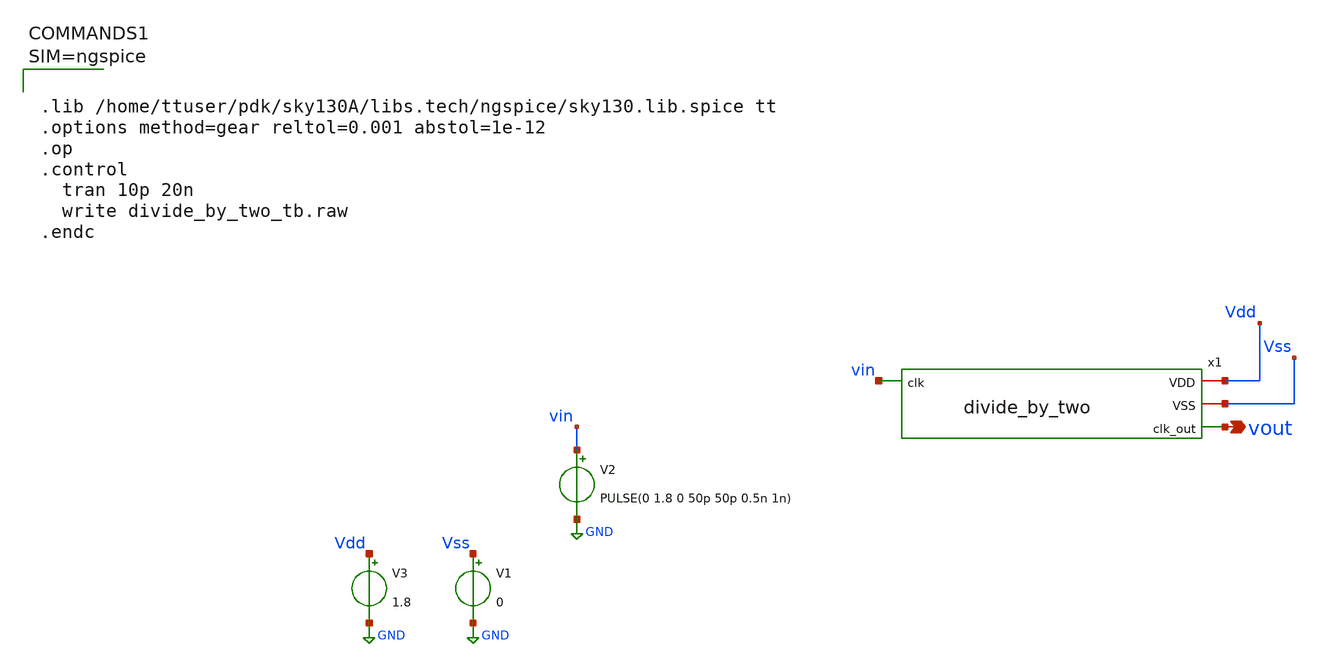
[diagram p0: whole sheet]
** sch_path: xschem/divide_by_two_tb.sch
**.subckt divide_by_two_tb vout
*.opin vout
V3 Vdd GND 1.8
V1 Vss GND 0
V2 vin GND PULSE(0 1.8 0 50p 50p 0.5n 1n)
x1 Vdd Vss vin vout divide_by_two
**** begin user architecture code



.lib /home/ttuser/pdk/sky130A/libs.tech/ngspice/sky130.lib.spice tt
.options method=gear reltol=0.001 abstol=1e-12
.op
.control
  tran 10p 20n
  write divide_by_two_tb.raw
.endc



**** end user architecture code
**.ends

* expanding   symbol:  divide_by_two.sym # of pins=4
** sym_path: xschem/divide_by_two.sym
** sch_path: xschem/divide_by_two.sch
.subckt divide_by_two VDD VSS clk clk_out
*.opin clk_out
*.ipin clk
*.iopin VDD
*.iopin VSS
XM1 net1 net6 VSS VSS sky130_fd_pr__nfet_01v8 L=0.15 W=1 nf=1 ad='int((nf+1)/2) * W/nf * 0.29' as='int((nf+2)/2) * W/nf * 0.29'
+ pd='2*int((nf+1)/2) * (W/nf + 0.29)' ps='2*int((nf+2)/2) * (W/nf + 0.29)' nrd='0.29 / W' nrs='0.29 / W'
+ sa=0 sb=0 sd=0 mult=1 m=1
XM2 net1 clk net2 VDD sky130_fd_pr__pfet_01v8 L=0.15 W=4 nf=1 ad='int((nf+1)/2) * W/nf * 0.29' as='int((nf+2)/2) * W/nf * 0.29'
+ pd='2*int((nf+1)/2) * (W/nf + 0.29)' ps='2*int((nf+2)/2) * (W/nf + 0.29)' nrd='0.29 / W' nrs='0.29 / W'
+ sa=0 sb=0 sd=0 mult=1 m=1
XM3 net2 net6 VDD VDD sky130_fd_pr__pfet_01v8 L=0.15 W=4 nf=1 ad='int((nf+1)/2) * W/nf * 0.29' as='int((nf+2)/2) * W/nf * 0.29'
+ pd='2*int((nf+1)/2) * (W/nf + 0.29)' ps='2*int((nf+2)/2) * (W/nf + 0.29)' nrd='0.29 / W' nrs='0.29 / W'
+ sa=0 sb=0 sd=0 mult=1 m=1
XM4 net3 clk VSS VSS sky130_fd_pr__nfet_01v8 L=0.15 W=1 nf=1 ad='int((nf+1)/2) * W/nf * 0.29' as='int((nf+2)/2) * W/nf * 0.29'
+ pd='2*int((nf+1)/2) * (W/nf + 0.29)' ps='2*int((nf+2)/2) * (W/nf + 0.29)' nrd='0.29 / W' nrs='0.29 / W'
+ sa=0 sb=0 sd=0 mult=1 m=1
XM6 net4 clk VDD VDD sky130_fd_pr__pfet_01v8 L=0.15 W=1 nf=1 ad='int((nf+1)/2) * W/nf * 0.29' as='int((nf+2)/2) * W/nf * 0.29'
+ pd='2*int((nf+1)/2) * (W/nf + 0.29)' ps='2*int((nf+2)/2) * (W/nf + 0.29)' nrd='0.29 / W' nrs='0.29 / W'
+ sa=0 sb=0 sd=0 mult=1 m=1
XM7 net5 net4 VSS VSS sky130_fd_pr__nfet_01v8 L=0.15 W=1 nf=1 ad='int((nf+1)/2) * W/nf * 0.29' as='int((nf+2)/2) * W/nf * 0.29'
+ pd='2*int((nf+1)/2) * (W/nf + 0.29)' ps='2*int((nf+2)/2) * (W/nf + 0.29)' nrd='0.29 / W' nrs='0.29 / W'
+ sa=0 sb=0 sd=0 mult=1 m=1
XM9 net6 net4 VDD VDD sky130_fd_pr__pfet_01v8 L=0.15 W=1 nf=1 ad='int((nf+1)/2) * W/nf * 0.29' as='int((nf+2)/2) * W/nf * 0.29'
+ pd='2*int((nf+1)/2) * (W/nf + 0.29)' ps='2*int((nf+2)/2) * (W/nf + 0.29)' nrd='0.29 / W' nrs='0.29 / W'
+ sa=0 sb=0 sd=0 mult=1 m=1
XM5 net4 net1 net3 VSS sky130_fd_pr__nfet_01v8 L=0.15 W=1 nf=1 ad='int((nf+1)/2) * W/nf * 0.29' as='int((nf+2)/2) * W/nf * 0.29'
+ pd='2*int((nf+1)/2) * (W/nf + 0.29)' ps='2*int((nf+2)/2) * (W/nf + 0.29)' nrd='0.29 / W' nrs='0.29 / W'
+ sa=0 sb=0 sd=0 mult=1 m=1
XM8 net6 clk net5 VSS sky130_fd_pr__nfet_01v8 L=0.15 W=1 nf=1 ad='int((nf+1)/2) * W/nf * 0.29' as='int((nf+2)/2) * W/nf * 0.29'
+ pd='2*int((nf+1)/2) * (W/nf + 0.29)' ps='2*int((nf+2)/2) * (W/nf + 0.29)' nrd='0.29 / W' nrs='0.29 / W'
+ sa=0 sb=0 sd=0 mult=1 m=1
XM10 clk_out net6 VDD VDD sky130_fd_pr__pfet_01v8 L=0.15 W=2 nf=1 ad='int((nf+1)/2) * W/nf * 0.29' as='int((nf+2)/2) * W/nf * 0.29'
+ pd='2*int((nf+1)/2) * (W/nf + 0.29)' ps='2*int((nf+2)/2) * (W/nf + 0.29)' nrd='0.29 / W' nrs='0.29 / W'
+ sa=0 sb=0 sd=0 mult=1 m=1
XM11 clk_out net6 VSS VSS sky130_fd_pr__nfet_01v8 L=0.15 W=1 nf=1 ad='int((nf+1)/2) * W/nf * 0.29' as='int((nf+2)/2) * W/nf * 0.29'
+ pd='2*int((nf+1)/2) * (W/nf + 0.29)' ps='2*int((nf+2)/2) * (W/nf + 0.29)' nrd='0.29 / W' nrs='0.29 / W'
+ sa=0 sb=0 sd=0 mult=1 m=1
.ends

.GLOBAL GND
.end
